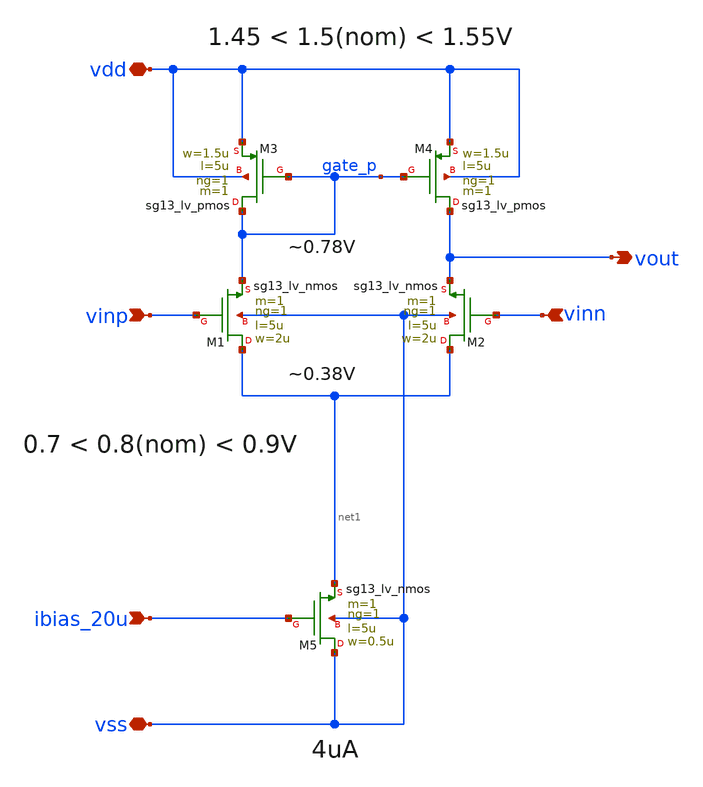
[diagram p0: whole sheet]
** sch_path: ic_design/2_Idealized_circuits/eaa/eaa_ota-5t.sch
* (c) 2024-2025 H. Pretl, Apache-2.0 license
**.subckt eaa_ota-5t ibias_20u vdd vss vinp vinn vout
*.ipin ibias_20u
*.iopin vdd
*.iopin vss
*.ipin vinp
*.ipin vinn
*.opin vout
XM5 vss ibias_20u net1 vss sg13_lv_nmos w=0.5u l=5u ng=1 m=1 mm_ok=1
XM4 vout gate_p vdd vdd sg13_lv_pmos w=1.5u l=5u ng=1 m=1 mm_ok=1
XM1 net1 vinp gate_p vss sg13_lv_nmos w=2u l=5u ng=1 m=1 mm_ok=1
XM2 net1 vinn vout vss sg13_lv_nmos w=2u l=5u ng=1 m=1 mm_ok=1
XM3 gate_p gate_p vdd vdd sg13_lv_pmos w=1.5u l=5u ng=1 m=1 mm_ok=1
**.ends
.end
